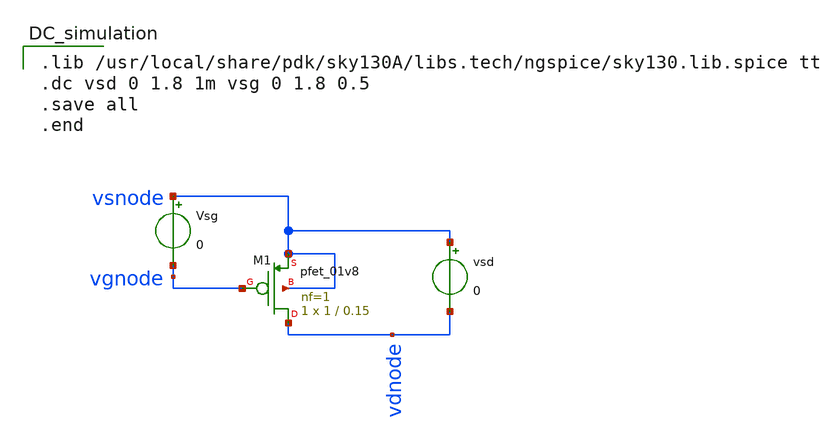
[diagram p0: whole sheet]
** sch_path: Xshem_files/dc_sweep_pmos.sch
**.subckt dc_sweep_pmos
XM1 vdnode vgnode vsnode vsnode sky130_fd_pr__pfet_01v8 L=0.15 W=1 nf=1 ad='int((nf+1)/2) * W/nf * 0.29'
+ as='int((nf+2)/2) * W/nf * 0.29' pd='2*int((nf+1)/2) * (W/nf + 0.29)' ps='2*int((nf+2)/2) * (W/nf + 0.29)'
+ nrd='0.29 / W' nrs='0.29 / W' sa=0 sb=0 sd=0 mult=1 m=1
Vsg vsnode vgnode 0
vsd vsnode vdnode 0
**** begin user architecture code

.lib /usr/local/share/pdk/sky130A/libs.tech/ngspice/sky130.lib.spice tt
.dc vsd 0 1.8 1m vsg 0 1.8 0.5
.save all
.end

**** end user architecture code
**.ends
.end
